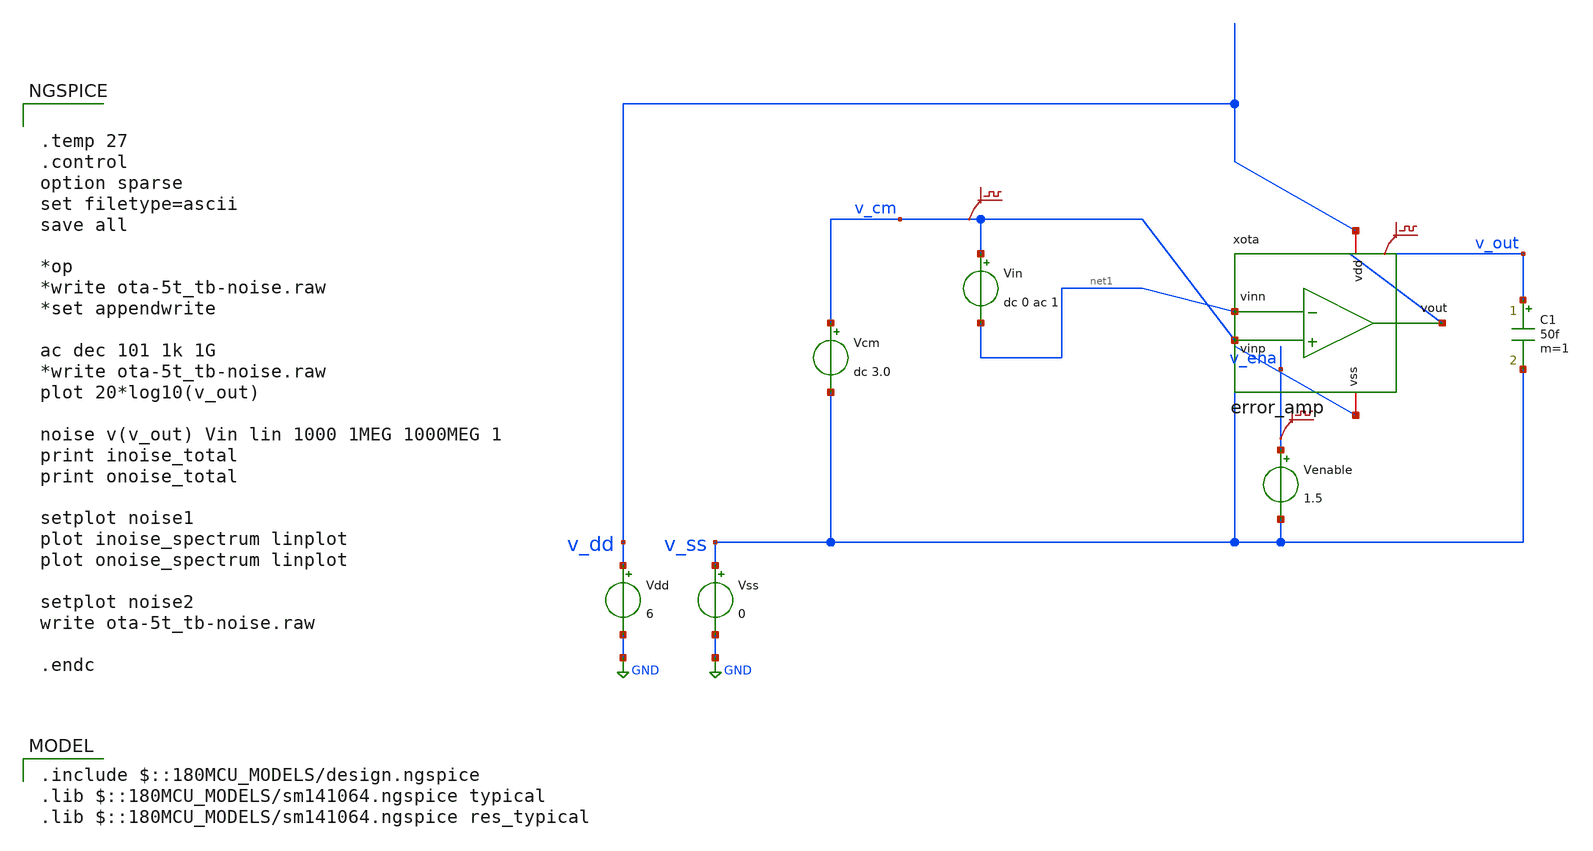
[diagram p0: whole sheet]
** sch_path: analog-db/drawings/ldo-005-ti-ldo-buffer-ref/gf180/error_amp/error_amp_tb-noise.sch
* (c) 2024-2025 H. Pretl, Apache-2.0 license
**.subckt error_amp_tb-noise
Vdd v_dd GND 6
xota v_dd v_out v_cm net1 v_ss error_amp
Vss v_ss GND 0
C1 v_out v_ss 50f m=1
Vcm v_cm v_ss dc 3.0
Venable v_ena v_ss 1.5
.save v(v_cm)
.save v(v_out)
.save v(v_ena)
Vin v_cm net1 dc 0 ac 1
**** begin user architecture code
 .include $::180MCU_MODELS/design.ngspice
.lib $::180MCU_MODELS/sm141064.ngspice typical
.lib $::180MCU_MODELS/sm141064.ngspice res_typical



.temp 27
.control
option sparse
set filetype=ascii
save all

*op
*write ota-5t_tb-noise.raw
*set appendwrite

ac dec 101 1k 1G
*write ota-5t_tb-noise.raw
plot 20*log10(v_out)

noise v(v_out) Vin lin 1000 1MEG 1000MEG 1
print inoise_total
print onoise_total

setplot noise1
plot inoise_spectrum linplot
plot onoise_spectrum linplot

setplot noise2
write ota-5t_tb-noise.raw

.endc


**** end user architecture code
**.ends

* expanding   symbol:  ldo-005-ti-ldo-buffer-ref/gf180/error_amp/error_amp.sym # of pins=5
** sym_path: analog-db/circuits/amp_032_ti_ldo_error_selfbias/pdk/gf180mcu/schematic/error_amp.sym
** sch_path: analog-db/circuits/amp_032_ti_ldo_error_selfbias/pdk/gf180mcu/schematic/error_amp.sch
.subckt error_amp vdd vout vinp vinn vss
*.iopin vdd
*.iopin vss
*.ipin vinp
*.opin vout
*.ipin vinn
XM2 net_b vinp net_c vss nfet_06v0 L=0.7u W=68.542u nf=1 ad='int((nf+1)/2) * W/nf * 0.18u' as='int((nf+2)/2) * W/nf * 0.18u'
+ pd='2*int((nf+1)/2) * (W/nf + 0.18u)' ps='2*int((nf+2)/2) * (W/nf + 0.18u)' nrd='0.18u / W' nrs='0.18u / W'
+ sa=0 sb=0 sd=0 m=1
XM3m net_a net_d vdd vdd pfet_06v0 L=0.5u W=69.545u nf=1 ad='int((nf+1)/2) * W/nf * 0.18u' as='int((nf+2)/2) * W/nf * 0.18u'
+ pd='2*int((nf+1)/2) * (W/nf + 0.18u)' ps='2*int((nf+2)/2) * (W/nf + 0.18u)' nrd='0.18u / W' nrs='0.18u / W'
+ sa=0 sb=0 sd=0 m=1
XM4 net_f net_a net_d vdd pfet_06v0 L=0.5u W=10u nf=1 ad='int((nf+1)/2) * W/nf * 0.18u' as='int((nf+2)/2) * W/nf * 0.18u'
+ pd='2*int((nf+1)/2) * (W/nf + 0.18u)' ps='2*int((nf+2)/2) * (W/nf + 0.18u)' nrd='0.18u / W' nrs='0.18u / W'
+ sa=0 sb=0 sd=0 m=1
XM5 net_b net_d vdd vdd pfet_06v0 L=0.5u W=69.545u nf=1 ad='int((nf+1)/2) * W/nf * 0.18u' as='int((nf+2)/2) * W/nf * 0.18u'
+ pd='2*int((nf+1)/2) * (W/nf + 0.18u)' ps='2*int((nf+2)/2) * (W/nf + 0.18u)' nrd='0.18u / W' nrs='0.18u / W'
+ sa=0 sb=0 sd=0 m=1
XM6 vout net_b vdd vdd pfet_06v0 L=3.8349u W=20u nf=1 ad='int((nf+1)/2) * W/nf * 0.18u' as='int((nf+2)/2) * W/nf * 0.18u'
+ pd='2*int((nf+1)/2) * (W/nf + 0.18u)' ps='2*int((nf+2)/2) * (W/nf + 0.18u)' nrd='0.18u / W' nrs='0.18u / W'
+ sa=0 sb=0 sd=0 m=1
Cc net1 vout 6.7168p m=1
XRZ net_b net1 vdd ppolyf_u_3k r_width=1u r_length=9.476u m=1
XM1 net_a vinn net_c vss nfet_06v0 L=0.7u W=68.542u nf=1 ad='int((nf+1)/2) * W/nf * 0.18u' as='int((nf+2)/2) * W/nf * 0.18u'
+ pd='2*int((nf+1)/2) * (W/nf + 0.18u)' ps='2*int((nf+2)/2) * (W/nf + 0.18u)' nrd='0.18u / W' nrs='0.18u / W'
+ sa=0 sb=0 sd=0 m=1
XM_mirror_error_amp_ref net2 net2 vss vss nfet_06v0 L=2u W=34.533u nf=1 ad='int((nf+1)/2) * W/nf * 0.18u'
+ as='int((nf+2)/2) * W/nf * 0.18u' pd='2*int((nf+1)/2) * (W/nf + 0.18u)' ps='2*int((nf+2)/2) * (W/nf + 0.18u)'
+ nrd='0.18u / W' nrs='0.18u / W' sa=0 sb=0 sd=0 m=1
XM_mirror_f net_f net2 vss vss nfet_06v0 L=2u W=5u nf=1 ad='int((nf+1)/2) * W/nf * 0.18u' as='int((nf+2)/2) * W/nf * 0.18u'
+ pd='2*int((nf+1)/2) * (W/nf + 0.18u)' ps='2*int((nf+2)/2) * (W/nf + 0.18u)' nrd='0.18u / W' nrs='0.18u / W'
+ sa=0 sb=0 sd=0 m=1
XM_mirror_c net_c net2 vss vss nfet_06v0 L=2u W=34.533u nf=1 ad='int((nf+1)/2) * W/nf * 0.18u' as='int((nf+2)/2) * W/nf * 0.18u'
+ pd='2*int((nf+1)/2) * (W/nf + 0.18u)' ps='2*int((nf+2)/2) * (W/nf + 0.18u)' nrd='0.18u / W' nrs='0.18u / W'
+ sa=0 sb=0 sd=0 m=1
XM_mirror_ea_out vout net2 vss vss nfet_06v0 L=2u W=34.533u nf=1 ad='int((nf+1)/2) * W/nf * 0.18u' as='int((nf+2)/2) * W/nf * 0.18u'
+ pd='2*int((nf+1)/2) * (W/nf + 0.18u)' ps='2*int((nf+2)/2) * (W/nf + 0.18u)' nrd='0.18u / W' nrs='0.18u / W'
+ sa=0 sb=0 sd=0 m=1
XM_bias net2 net2 vdd vdd pfet_06v0 L=2u W=6.3111u nf=1 ad='int((nf+1)/2) * W/nf * 0.18u' as='int((nf+2)/2) * W/nf * 0.18u'
+ pd='2*int((nf+1)/2) * (W/nf + 0.18u)' ps='2*int((nf+2)/2) * (W/nf + 0.18u)' nrd='0.18u / W' nrs='0.18u / W'
+ sa=0 sb=0 sd=0 m=1
.ends

.GLOBAL GND
.end
